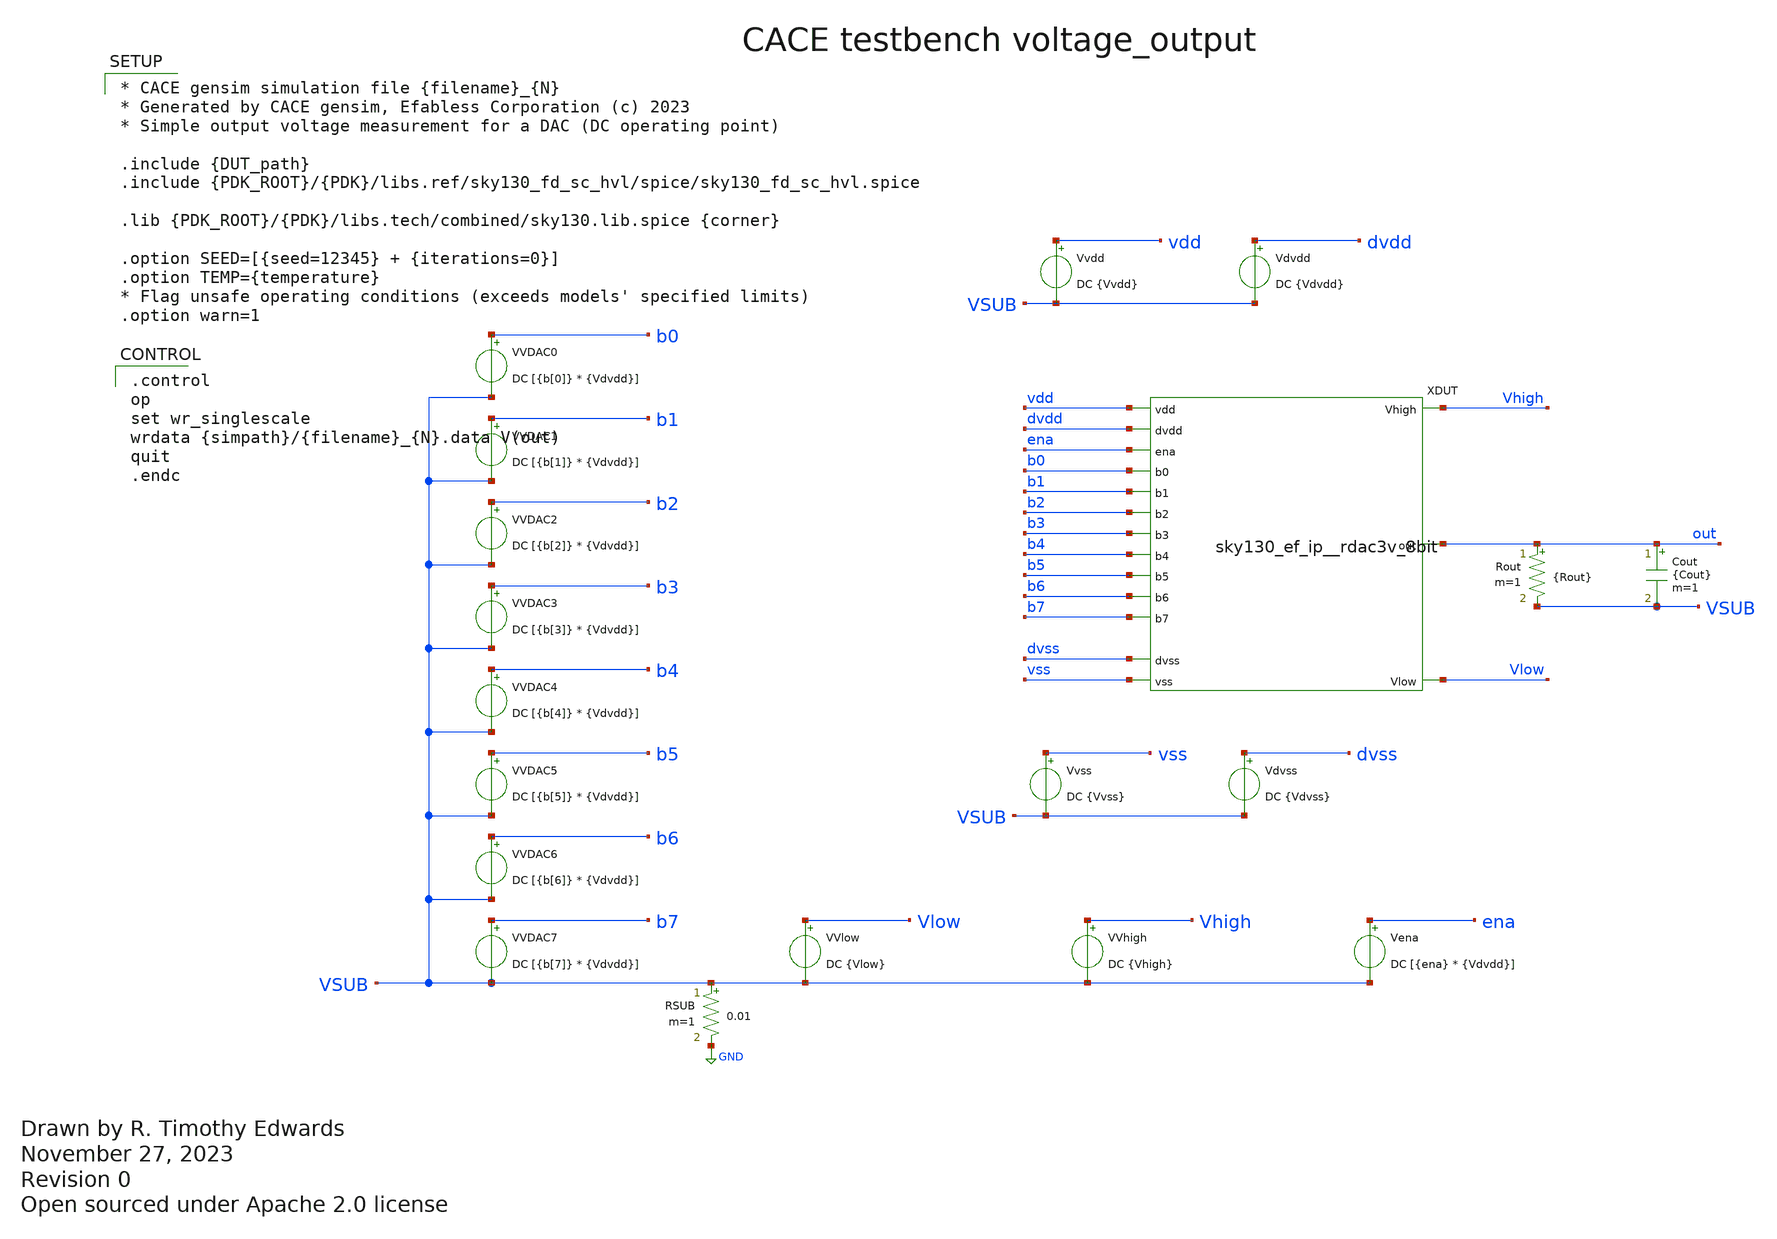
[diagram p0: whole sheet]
** sch_path: cace/voltage_output.sch
* Open sourced under Apache 2.0 license
**.subckt voltage_output
VVDAC7 b7 VSUB DC [{b[7]} * {Vdvdd}]
VVDAC1 b1 VSUB DC [{b[1]} * {Vdvdd}]
VVDAC2 b2 VSUB DC [{b[2]} * {Vdvdd}]
VVDAC3 b3 VSUB DC [{b[3]} * {Vdvdd}]
VVDAC4 b4 VSUB DC [{b[4]} * {Vdvdd}]
VVDAC5 b5 VSUB DC [{b[5]} * {Vdvdd}]
VVDAC6 b6 VSUB DC [{b[6]} * {Vdvdd}]
VVDAC0 b0 VSUB DC [{b[0]} * {Vdvdd}]
VVlow Vlow VSUB DC {Vlow}
VVhigh Vhigh VSUB DC {Vhigh}
Vena ena VSUB DC [{ena} * {Vdvdd}]
Vvss vss VSUB DC {Vvss}
Rout out VSUB {Rout} m=1
Cout out VSUB {Cout} m=1
Vdvss dvss VSUB DC {Vdvss}
Vvdd vdd VSUB DC {Vvdd}
Vdvdd dvdd VSUB DC {Vdvdd}
RSUB VSUB GND 0.01 m=1
XDUT dvdd vss dvss vdd b0 Vhigh b1 b2 b3 out b4 b5 ena b6 b7 Vlow sky130_ef_ip__rdac3v_8bit
**** begin user architecture code

.control
op
set wr_singlescale
wrdata {simpath}/{filename}_{N}.data V(out)
quit
.endc



* CACE gensim simulation file {filename}_{N}
* Generated by CACE gensim, Efabless Corporation (c) 2023
* Simple output voltage measurement for a DAC (DC operating point)

.include {DUT_path}
.include {PDK_ROOT}/{PDK}/libs.ref/sky130_fd_sc_hvl/spice/sky130_fd_sc_hvl.spice

.lib {PDK_ROOT}/{PDK}/libs.tech/combined/sky130.lib.spice {corner}

.option SEED=[{seed=12345} + {iterations=0}]
.option TEMP={temperature}
* Flag unsafe operating conditions (exceeds models' specified limits)
.option warn=1


**** end user architecture code
**.ends
.GLOBAL GND
.end
